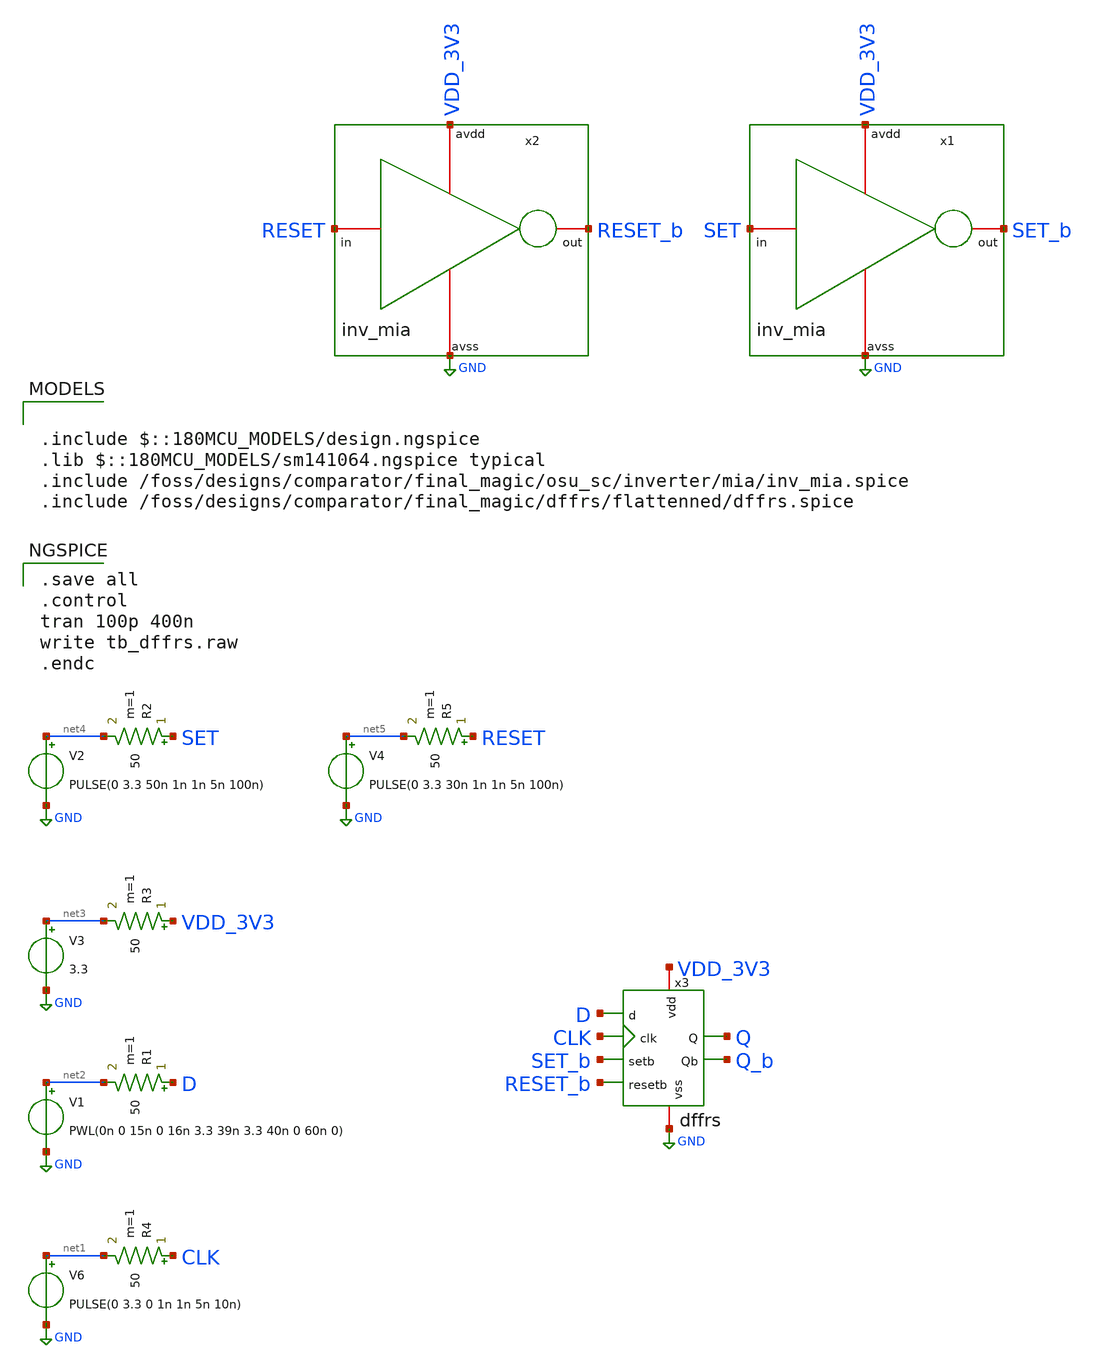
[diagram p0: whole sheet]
** sch_path: designs/FinalBlocksLayout/dffrs/flattened/tb_dffrs.sch
**.subckt tb_dffrs
V6 net1 GND PULSE(0 3.3 0 1n 1n 5n 10n)
R4 CLK net1 50 m=1
V1 net2 GND PWL(0n 0 15n 0 16n 3.3 39n 3.3 40n 0 60n 0)
R1 D net2 50 m=1
V3 net3 GND 3.3
R3 VDD_3V3 net3 50 m=1
V2 net4 GND PULSE(0 3.3 50n 1n 1n 5n 100n)
R2 SET net4 50 m=1
V4 net5 GND PULSE(0 3.3 30n 1n 1n 5n 100n)
R5 RESET net5 50 m=1
x2 VDD_3V3 RESET RESET_b GND inv_mia
x1 VDD_3V3 SET SET_b GND inv_mia
x3 VDD_3V3 GND D CLK SET_b RESET_b Q Q_b dffrs
**** begin user architecture code

.include $::180MCU_MODELS/design.ngspice
.lib $::180MCU_MODELS/sm141064.ngspice typical
.include /foss/designs/comparator/final_magic/osu_sc/inverter/mia/inv_mia.spice
.include /foss/designs/comparator/final_magic/dffrs/flattenned/dffrs.spice


.save all
.control
tran 100p 400n
write tb_dffrs.raw
.endc

**** end user architecture code
**.ends
.GLOBAL GND
.end
